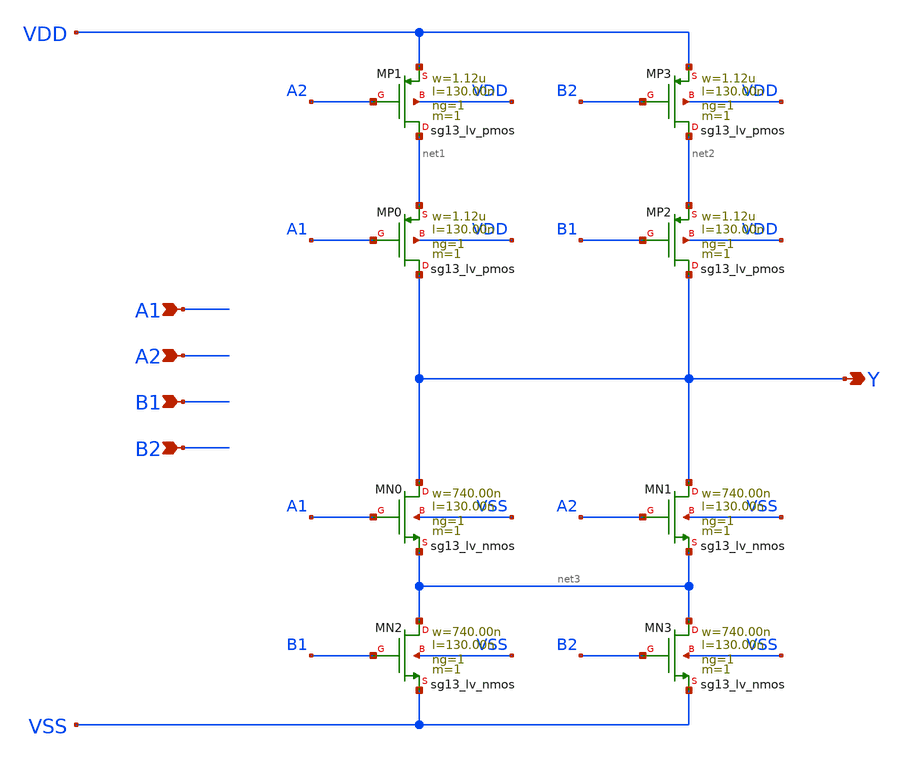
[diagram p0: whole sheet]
** sch_path: outputs/sg13g2_cells/cells/sg13g2_o22ai_1/sg13g2_o22ai_1.sch
**.subckt sg13g2_o22ai_1 A1 A2 B1 B2 Y
*.ipin A1
*.ipin A2
*.ipin B1
*.ipin B2
*.opin Y
XMN0 Y A1 net3 VSS sg13_lv_nmos w=740.00n l=130.00n ng=1 m=1 mm_ok=1
XMN1 Y A2 net3 VSS sg13_lv_nmos w=740.00n l=130.00n ng=1 m=1 mm_ok=1
XMN2 net3 B1 VSS VSS sg13_lv_nmos w=740.00n l=130.00n ng=1 m=1 mm_ok=1
XMN3 net3 B2 VSS VSS sg13_lv_nmos w=740.00n l=130.00n ng=1 m=1 mm_ok=1
XMP0 Y A1 net1 VDD sg13_lv_pmos w=1.12u l=130.00n ng=1 m=1 mm_ok=1
XMP1 net1 A2 VDD VDD sg13_lv_pmos w=1.12u l=130.00n ng=1 m=1 mm_ok=1
XMP2 Y B1 net2 VDD sg13_lv_pmos w=1.12u l=130.00n ng=1 m=1 mm_ok=1
XMP3 net2 B2 VDD VDD sg13_lv_pmos w=1.12u l=130.00n ng=1 m=1 mm_ok=1
**.ends
.end
